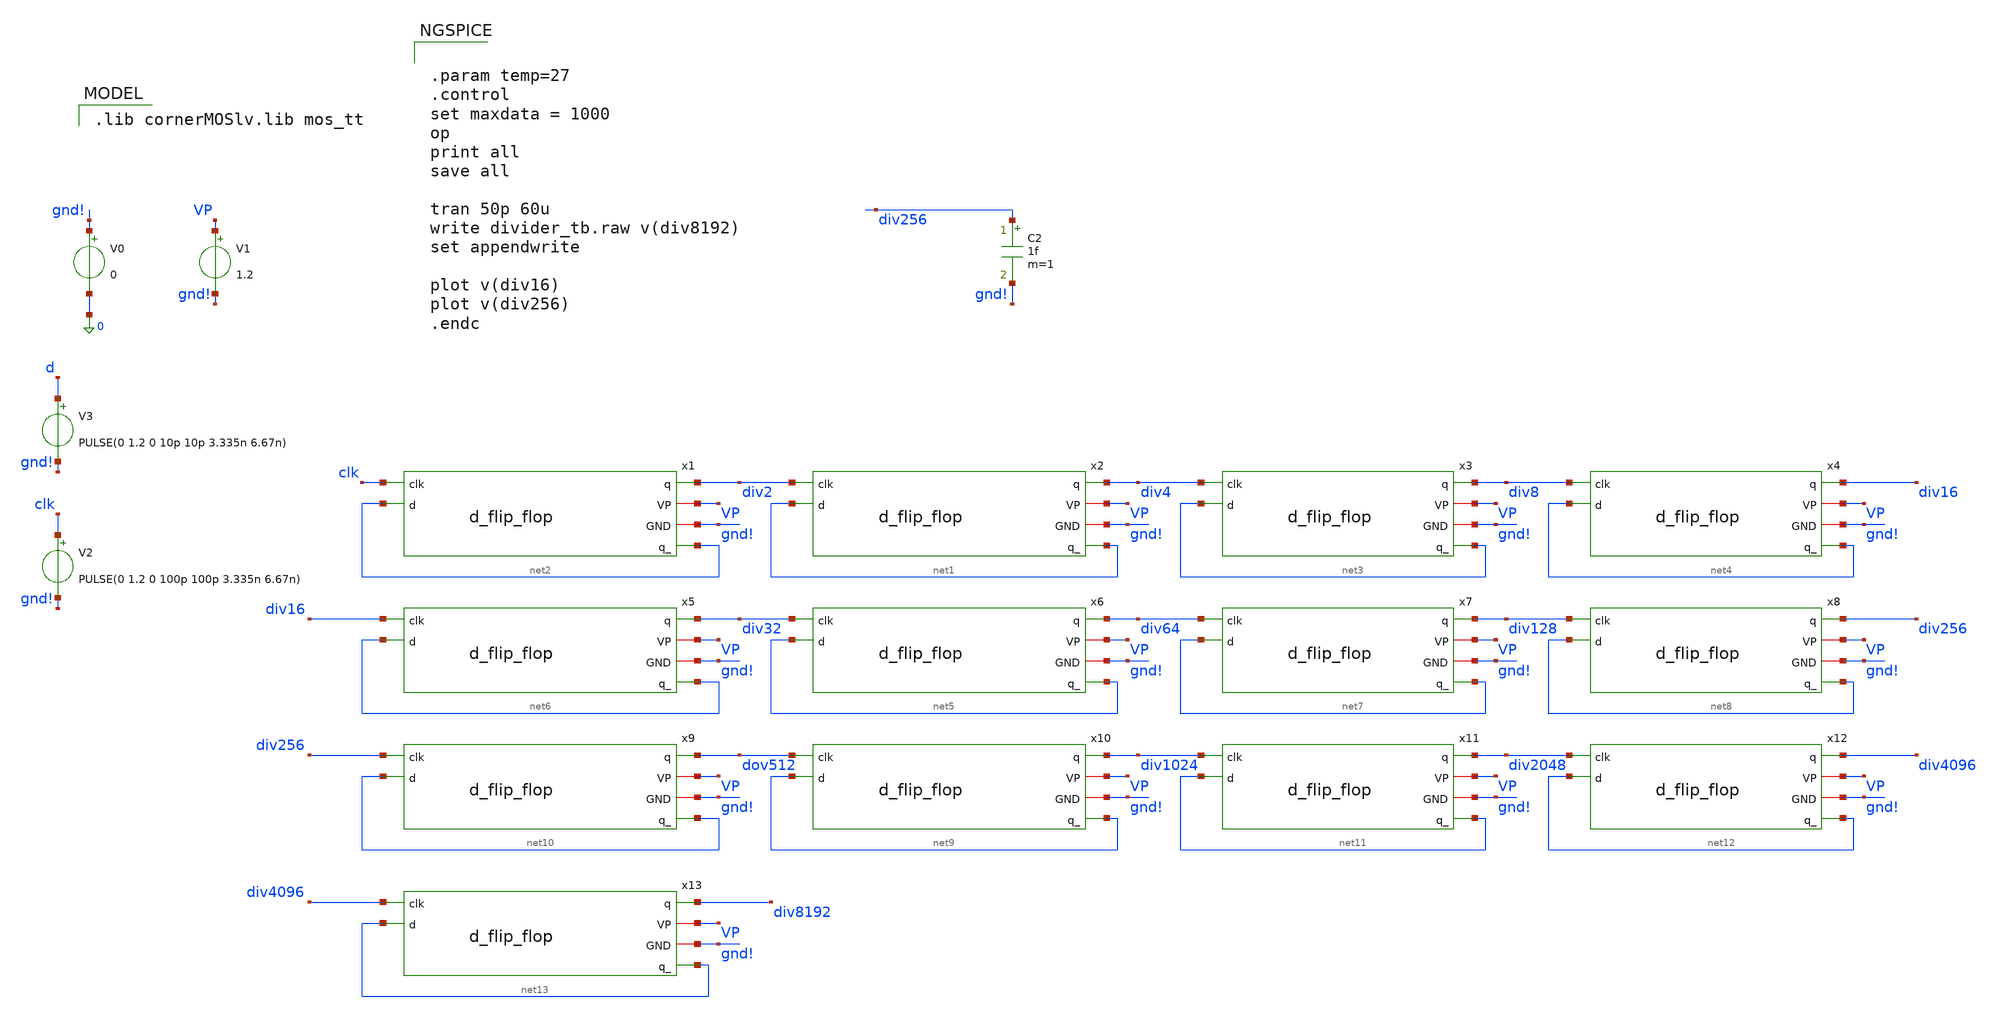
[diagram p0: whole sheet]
** sch_path: PLL0663-main/testbenches/tran/xschem/divider/divider_tb.sch
**.subckt divider_tb
V1 VP gnd! 1.2
V2 clk gnd! PULSE(0 1.2 0 100p 100p 3.335n 6.67n)
V0 gnd! 0 0
C2 div256 gnd! 1f m=1
x1 div2 VP gnd! net2 clk net2 d_flip_flop
x2 div4 VP gnd! net1 div2 net1 d_flip_flop
x3 div8 VP gnd! net3 div4 net3 d_flip_flop
x4 div16 VP gnd! net4 div8 net4 d_flip_flop
x5 div32 VP gnd! net6 div16 net6 d_flip_flop
x6 div64 VP gnd! net5 div32 net5 d_flip_flop
x7 div128 VP gnd! net7 div64 net7 d_flip_flop
x8 div256 VP gnd! net8 div128 net8 d_flip_flop
V3 d gnd! PULSE(0 1.2 0 10p 10p 3.335n 6.67n)
x9 dov512 VP gnd! net10 div256 net10 d_flip_flop
x10 div1024 VP gnd! net9 dov512 net9 d_flip_flop
x11 div2048 VP gnd! net11 div1024 net11 d_flip_flop
x12 div4096 VP gnd! net12 div2048 net12 d_flip_flop
x13 div8192 VP gnd! net13 div4096 net13 d_flip_flop
**** begin user architecture code
 .lib cornerMOSlv.lib mos_tt



.param temp=27
.control
set maxdata = 1000
op
print all
save all

tran 50p 60u
write divider_tb.raw v(div8192)
set appendwrite

plot v(div16)
plot v(div256)
.endc


**** end user architecture code
**.ends
.end
